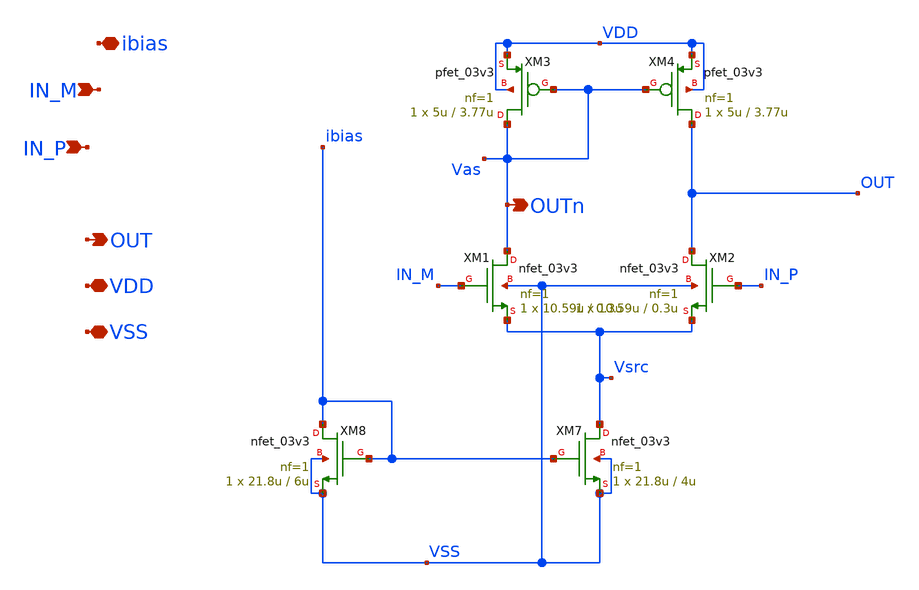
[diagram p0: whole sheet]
** sch_path: SAR_ADC/xschem/designs/stat_preamp.sch
**.subckt stat_preamp IN_M IN_P OUT VDD VSS ibias OUTn
*.ipin IN_M
*.ipin IN_P
*.opin OUT
*.iopin VDD
*.iopin VSS
*.iopin ibias
*.opin OUTn
XM3 Vas Vas VDD VDD pfet_03v3 L=3.77u W=5u nf=1 ad='int((nf+1)/2) * W/nf * 0.18u' as='int((nf+2)/2) * W/nf * 0.18u'
+ pd='2*int((nf+1)/2) * (W/nf + 0.18u)' ps='2*int((nf+2)/2) * (W/nf + 0.18u)' nrd='0.18u / W' nrs='0.18u / W'
+ sa=0 sb=0 sd=0 m=1
XM1 Vas IN_M Vsrc VSS nfet_03v3 L=0.3u W=10.59u nf=1 ad='int((nf+1)/2) * W/nf * 0.18u' as='int((nf+2)/2) * W/nf * 0.18u'
+ pd='2*int((nf+1)/2) * (W/nf + 0.18u)' ps='2*int((nf+2)/2) * (W/nf + 0.18u)' nrd='0.18u / W' nrs='0.18u / W'
+ sa=0 sb=0 sd=0 m=1
XM2 OUT IN_P Vsrc VSS nfet_03v3 L=0.3u W=10.59u nf=1 ad='int((nf+1)/2) * W/nf * 0.18u' as='int((nf+2)/2) * W/nf * 0.18u'
+ pd='2*int((nf+1)/2) * (W/nf + 0.18u)' ps='2*int((nf+2)/2) * (W/nf + 0.18u)' nrd='0.18u / W' nrs='0.18u / W'
+ sa=0 sb=0 sd=0 m=1
XM7 Vsrc ibias VSS VSS nfet_03v3 L=4u W=21.8u nf=1 ad='int((nf+1)/2) * W/nf * 0.18u' as='int((nf+2)/2) * W/nf * 0.18u'
+ pd='2*int((nf+1)/2) * (W/nf + 0.18u)' ps='2*int((nf+2)/2) * (W/nf + 0.18u)' nrd='0.18u / W' nrs='0.18u / W'
+ sa=0 sb=0 sd=0 m=1
XM8 ibias ibias VSS VSS nfet_03v3 L=6u W=21.8u nf=1 ad='int((nf+1)/2) * W/nf * 0.18u' as='int((nf+2)/2) * W/nf * 0.18u'
+ pd='2*int((nf+1)/2) * (W/nf + 0.18u)' ps='2*int((nf+2)/2) * (W/nf + 0.18u)' nrd='0.18u / W' nrs='0.18u / W'
+ sa=0 sb=0 sd=0 m=1
XM4 OUT Vas VDD VDD pfet_03v3 L=3.77u W=5u nf=1 ad='int((nf+1)/2) * W/nf * 0.18u' as='int((nf+2)/2) * W/nf * 0.18u'
+ pd='2*int((nf+1)/2) * (W/nf + 0.18u)' ps='2*int((nf+2)/2) * (W/nf + 0.18u)' nrd='0.18u / W' nrs='0.18u / W'
+ sa=0 sb=0 sd=0 m=1
**.ends
.end
